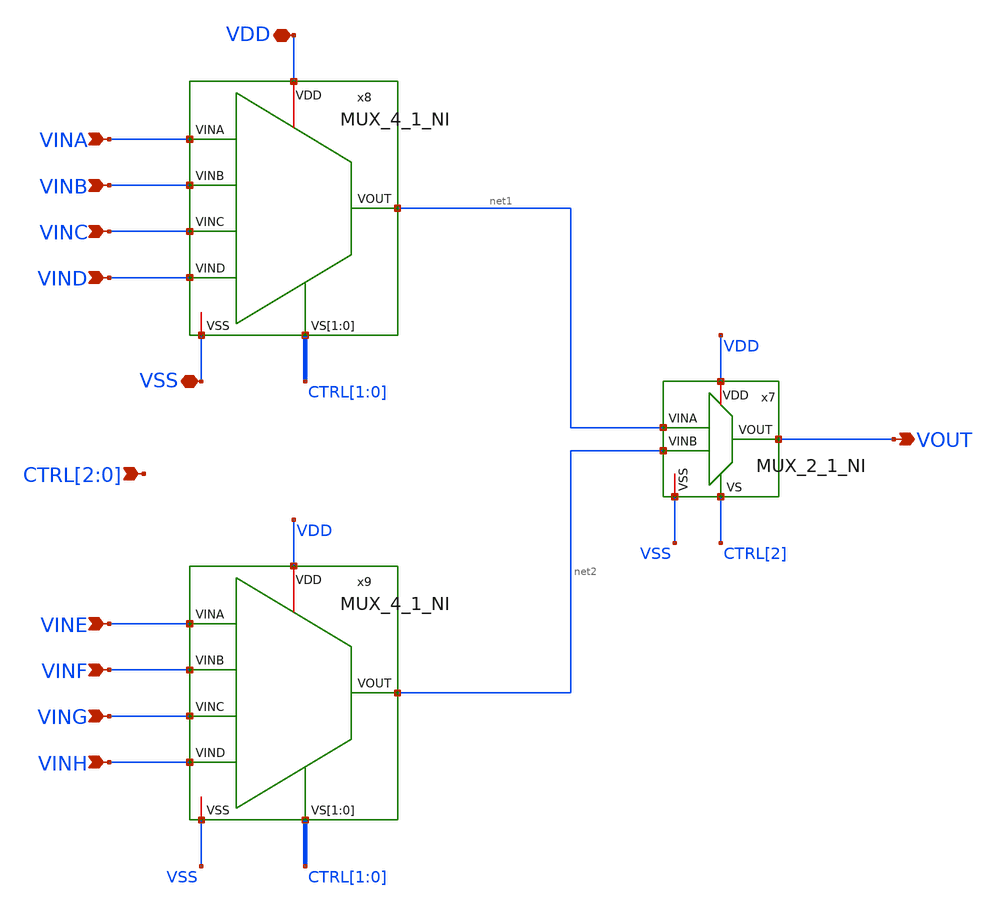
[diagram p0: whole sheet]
** sch_path: ADC8711-main/schematic/xschem/MUX_8_1_NI.sch
**.subckt MUX_8_1_NI VSS VOUT VDD VINA VINB VINC VIND CTRL[2],CTRL[1],CTRL[0] VINE VINF VING VINH
*.iopin VSS
*.opin VOUT
*.iopin VDD
*.ipin VINA
*.ipin VINB
*.ipin VINC
*.ipin VIND
*.ipin CTRL[2],CTRL[1],CTRL[0]
*.ipin VINE
*.ipin VINF
*.ipin VING
*.ipin VINH
x7 VDD net1 VOUT CTRL[2] net2 VSS MUX_2_1_NI
x8 VINA VINB VDD net1 CTRL[1] CTRL[0] VINC VSS VIND MUX_4_1_NI
x9 VINE VINF VDD net2 CTRL[1] CTRL[0] VING VSS VINH MUX_4_1_NI
**.ends
.end
